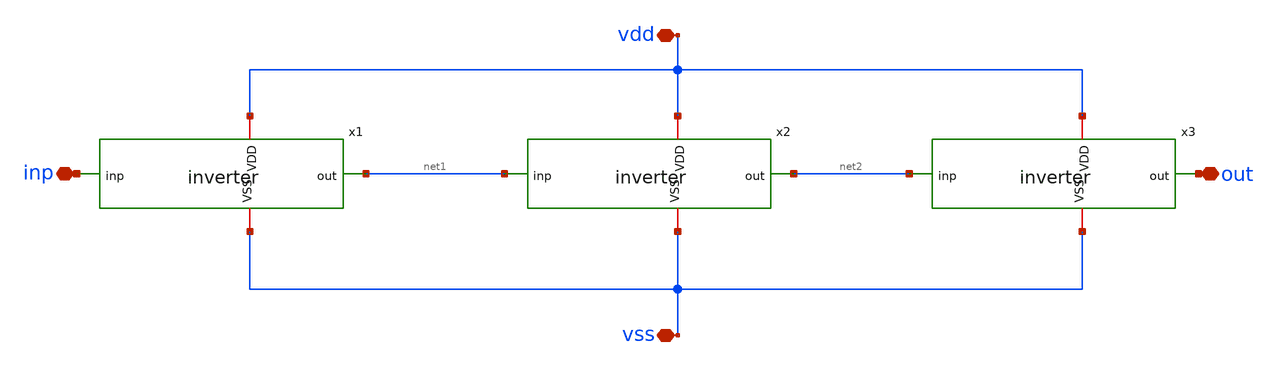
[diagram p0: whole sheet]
** sch_path: xschem01/inverter/inverter_chain.sch
**.subckt inverter_chain vdd vss inp out
*.iopin vdd
*.iopin vss
*.iopin inp
*.iopin out
x1 vdd inp net1 vss inverter
x2 vdd net1 net2 vss inverter
x3 vdd net2 out vss inverter
**.ends

* expanding   symbol:  /home/vks/pll/xschem01/inverter/inverter.sym # of pins=4
** sym_path: xschem01/inverter/inverter.sym
** sch_path: xschem01/inverter/inverter.sch
.subckt inverter VDD inp out VSS
*.ipin inp
*.opin out
*.iopin VDD
*.iopin VSS
x4 inp VSS VSS VDD VDD out sky130_fd_sc_hd__inv_4
.ends

.end
